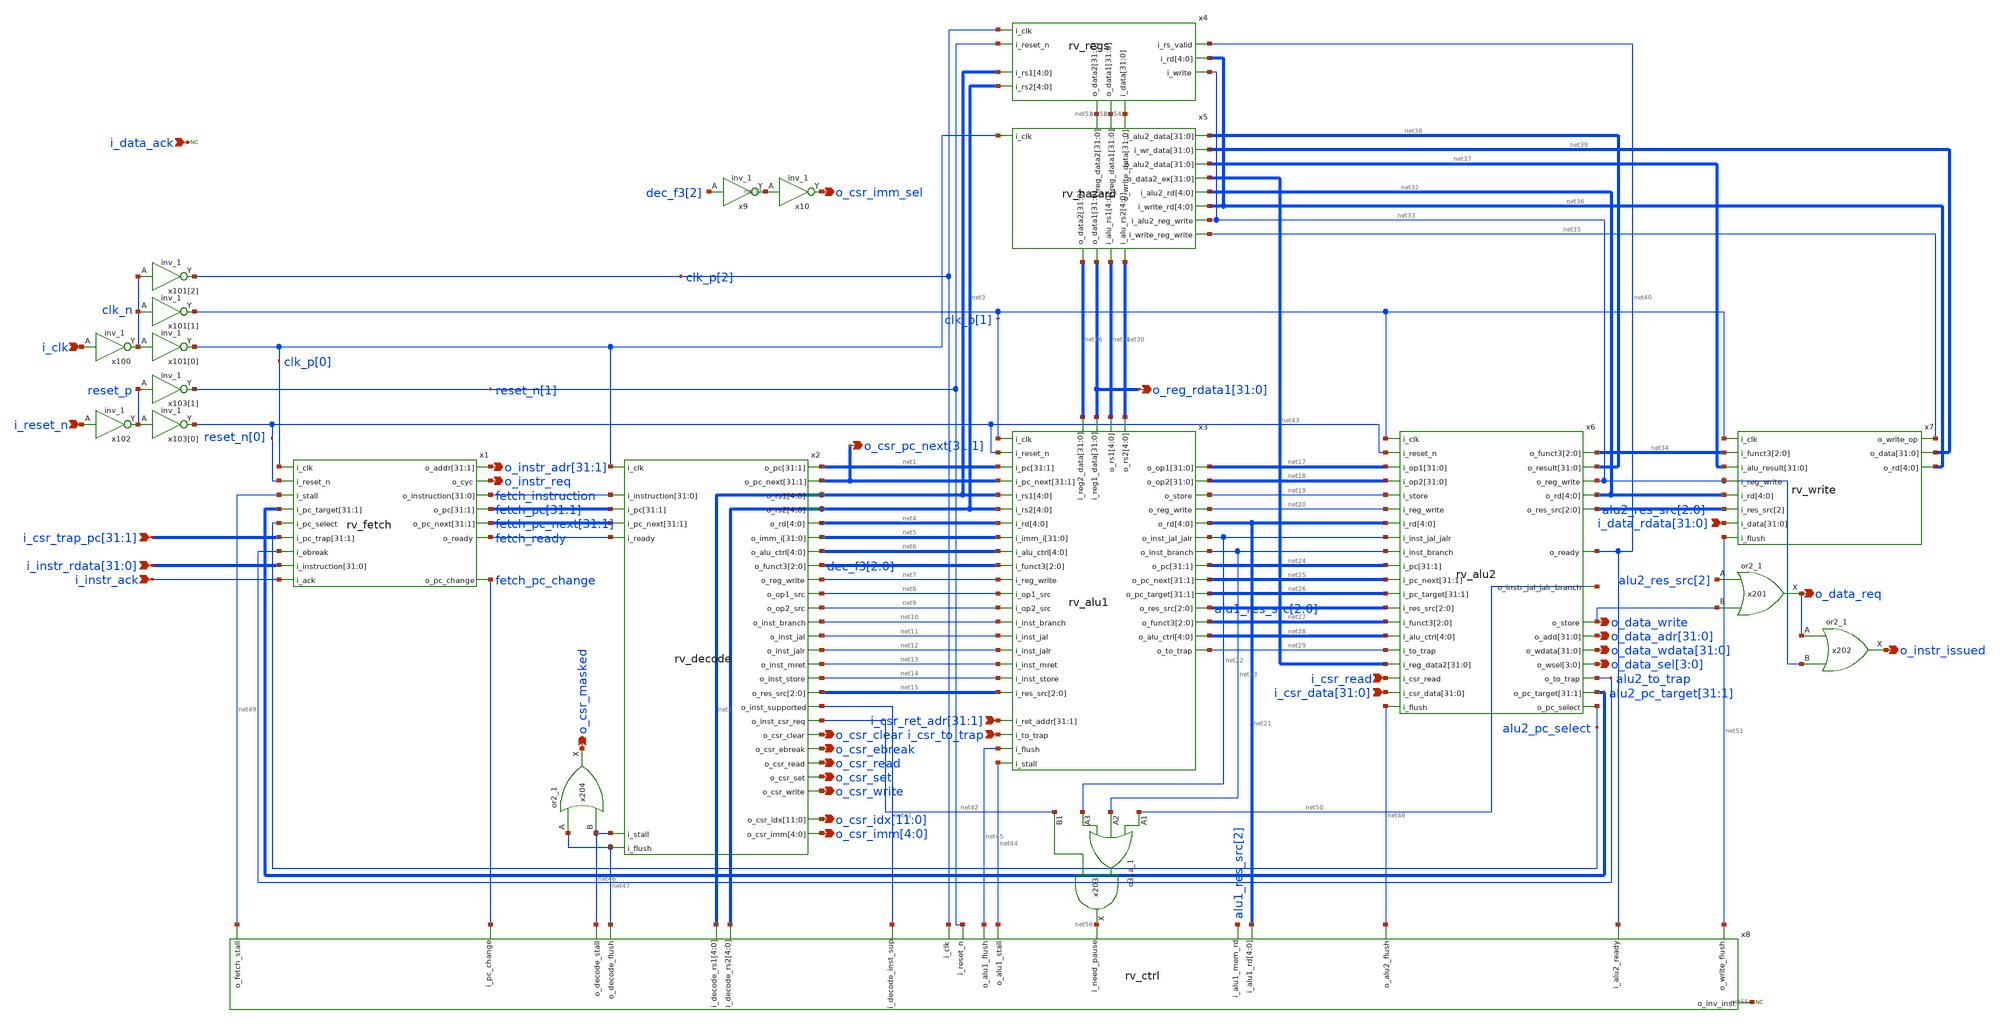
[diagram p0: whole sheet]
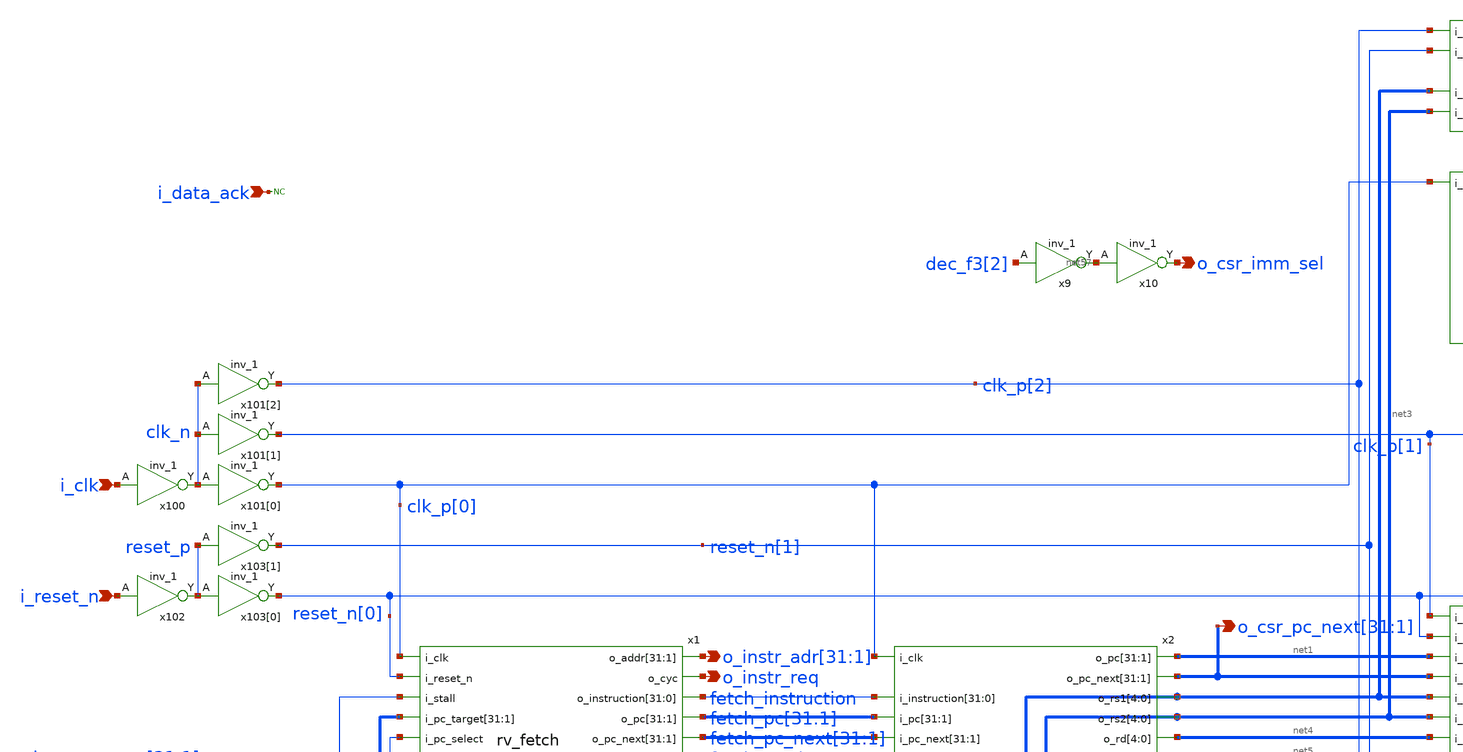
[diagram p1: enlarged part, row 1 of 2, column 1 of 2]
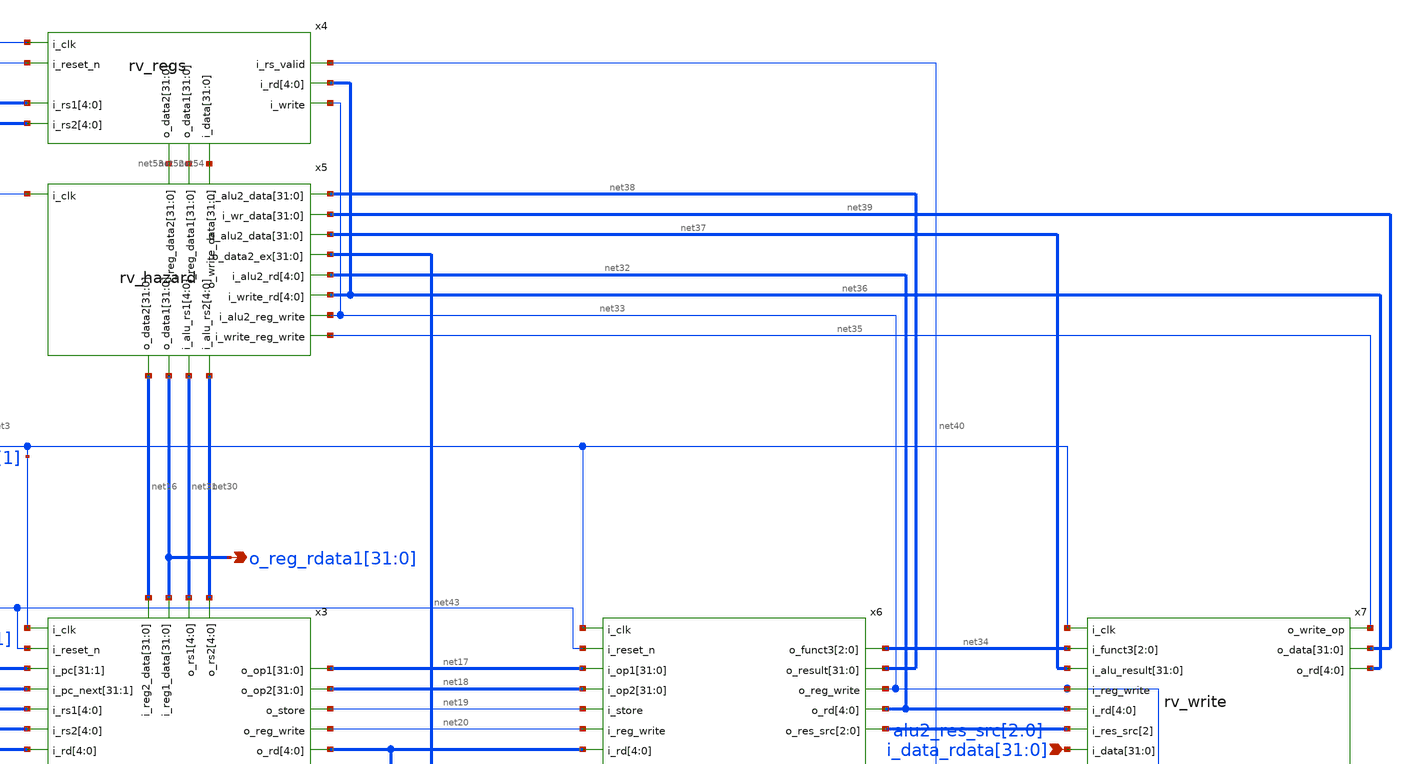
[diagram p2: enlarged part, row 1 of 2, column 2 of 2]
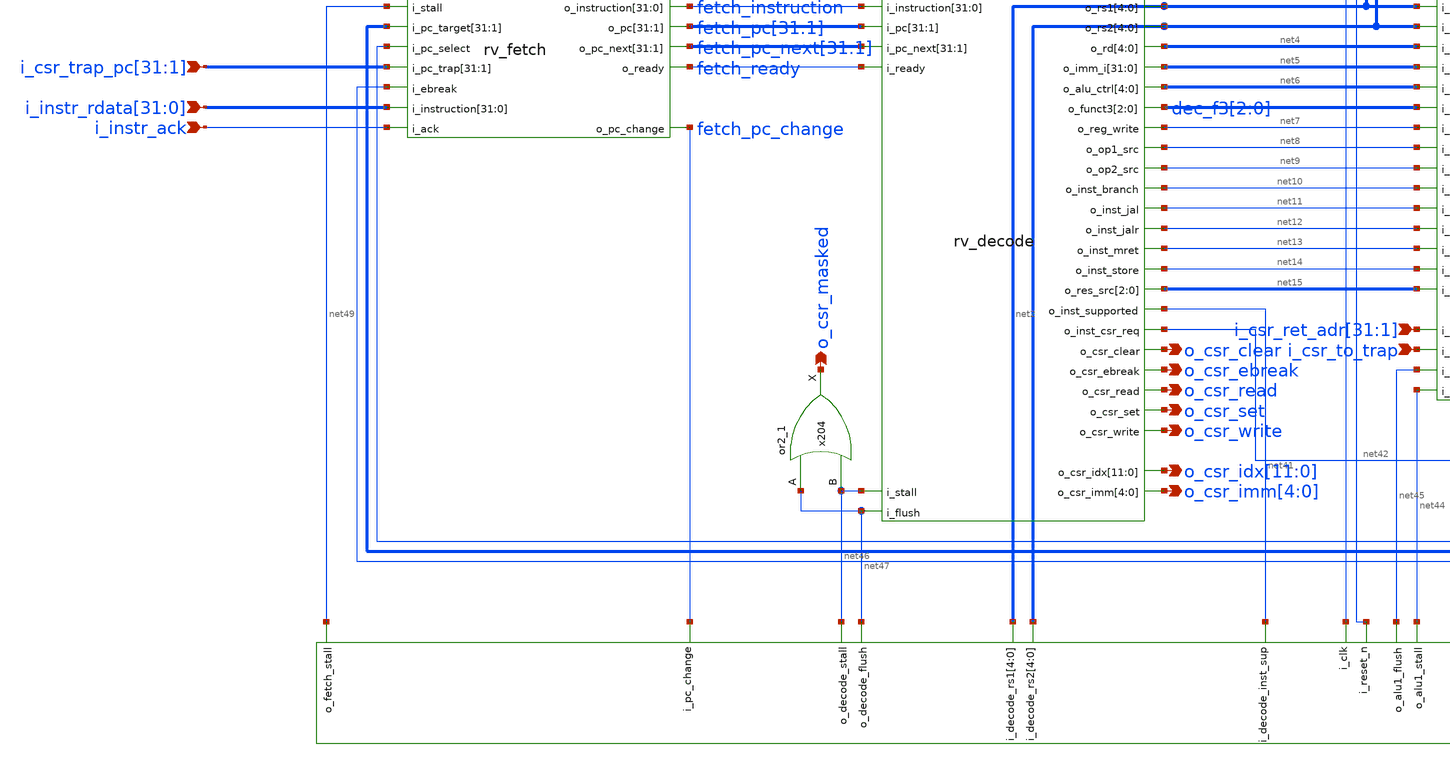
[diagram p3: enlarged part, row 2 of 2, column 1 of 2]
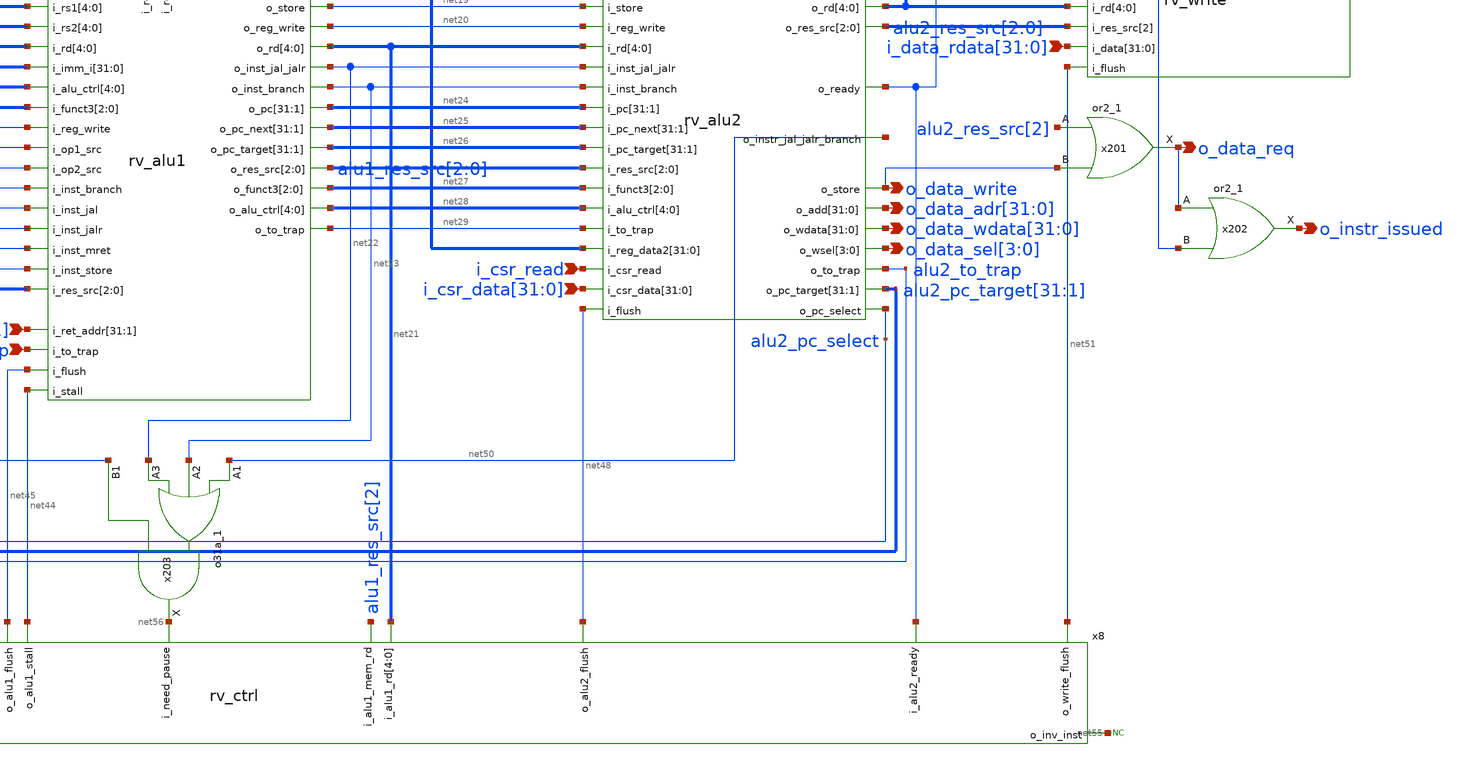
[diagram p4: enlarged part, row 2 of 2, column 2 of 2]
** sch_path: blocks/rv_core/rv_core.sch
**.subckt rv_core i_clk i_reset_n i_csr_read o_csr_clear o_data_req
*+ o_data_wdata[31],o_data_wdata[30],o_data_wdata[29],o_data_wdata[28],o_data_wdata[27],o_data_wdata[26],o_data_wdata[25],o_data_wdata[24],o_data_wdata[23],o_data_wdata[22],o_data_wdata[21],o_data_wdata[20],o_data_wdata[19],o_data_wdata[18],o_data_wdata[17],o_data_wdata[16],o_data_wdata[15],o_data_wdata[14],o_data_wdata[13],o_data_wdata[12],o_data_wdata[11],o_data_wdata[10],o_data_wdata[9],o_data_wdata[8],o_data_wdata[7],o_data_wdata[6],o_data_wdata[5],o_data_wdata[4],o_data_wdata[3],o_data_wdata[2],o_data_wdata[1],o_data_wdata[0] o_instr_issued
*+ o_data_adr[31],o_data_adr[30],o_data_adr[29],o_data_adr[28],o_data_adr[27],o_data_adr[26],o_data_adr[25],o_data_adr[24],o_data_adr[23],o_data_adr[22],o_data_adr[21],o_data_adr[20],o_data_adr[19],o_data_adr[18],o_data_adr[17],o_data_adr[16],o_data_adr[15],o_data_adr[14],o_data_adr[13],o_data_adr[12],o_data_adr[11],o_data_adr[10],o_data_adr[9],o_data_adr[8],o_data_adr[7],o_data_adr[6],o_data_adr[5],o_data_adr[4],o_data_adr[3],o_data_adr[2],o_data_adr[1],o_data_adr[0] o_data_sel[3],o_data_sel[2],o_data_sel[1],o_data_sel[0]
*+ i_csr_data[31],i_csr_data[30],i_csr_data[29],i_csr_data[28],i_csr_data[27],i_csr_data[26],i_csr_data[25],i_csr_data[24],i_csr_data[23],i_csr_data[22],i_csr_data[21],i_csr_data[20],i_csr_data[19],i_csr_data[18],i_csr_data[17],i_csr_data[16],i_csr_data[15],i_csr_data[14],i_csr_data[13],i_csr_data[12],i_csr_data[11],i_csr_data[10],i_csr_data[9],i_csr_data[8],i_csr_data[7],i_csr_data[6],i_csr_data[5],i_csr_data[4],i_csr_data[3],i_csr_data[2],i_csr_data[1],i_csr_data[0] i_csr_to_trap o_csr_ebreak o_csr_read o_csr_set o_csr_write o_csr_imm_sel
*+ i_csr_ret_adr[31],i_csr_ret_adr[30],i_csr_ret_adr[29],i_csr_ret_adr[28],i_csr_ret_adr[27],i_csr_ret_adr[26],i_csr_ret_adr[25],i_csr_ret_adr[24],i_csr_ret_adr[23],i_csr_ret_adr[22],i_csr_ret_adr[21],i_csr_ret_adr[20],i_csr_ret_adr[19],i_csr_ret_adr[18],i_csr_ret_adr[17],i_csr_ret_adr[16],i_csr_ret_adr[15],i_csr_ret_adr[14],i_csr_ret_adr[13],i_csr_ret_adr[12],i_csr_ret_adr[11],i_csr_ret_adr[10],i_csr_ret_adr[9],i_csr_ret_adr[8],i_csr_ret_adr[7],i_csr_ret_adr[6],i_csr_ret_adr[5],i_csr_ret_adr[4],i_csr_ret_adr[3],i_csr_ret_adr[2],i_csr_ret_adr[1]
*+ i_csr_trap_pc[31],i_csr_trap_pc[30],i_csr_trap_pc[29],i_csr_trap_pc[28],i_csr_trap_pc[27],i_csr_trap_pc[26],i_csr_trap_pc[25],i_csr_trap_pc[24],i_csr_trap_pc[23],i_csr_trap_pc[22],i_csr_trap_pc[21],i_csr_trap_pc[20],i_csr_trap_pc[19],i_csr_trap_pc[18],i_csr_trap_pc[17],i_csr_trap_pc[16],i_csr_trap_pc[15],i_csr_trap_pc[14],i_csr_trap_pc[13],i_csr_trap_pc[12],i_csr_trap_pc[11],i_csr_trap_pc[10],i_csr_trap_pc[9],i_csr_trap_pc[8],i_csr_trap_pc[7],i_csr_trap_pc[6],i_csr_trap_pc[5],i_csr_trap_pc[4],i_csr_trap_pc[3],i_csr_trap_pc[2],i_csr_trap_pc[1]
*+ o_csr_idx[11],o_csr_idx[10],o_csr_idx[9],o_csr_idx[8],o_csr_idx[7],o_csr_idx[6],o_csr_idx[5],o_csr_idx[4],o_csr_idx[3],o_csr_idx[2],o_csr_idx[1],o_csr_idx[0] o_csr_imm[4],o_csr_imm[3],o_csr_imm[2],o_csr_imm[1],o_csr_imm[0]
*+ o_csr_pc_next[31],o_csr_pc_next[30],o_csr_pc_next[29],o_csr_pc_next[28],o_csr_pc_next[27],o_csr_pc_next[26],o_csr_pc_next[25],o_csr_pc_next[24],o_csr_pc_next[23],o_csr_pc_next[22],o_csr_pc_next[21],o_csr_pc_next[20],o_csr_pc_next[19],o_csr_pc_next[18],o_csr_pc_next[17],o_csr_pc_next[16],o_csr_pc_next[15],o_csr_pc_next[14],o_csr_pc_next[13],o_csr_pc_next[12],o_csr_pc_next[11],o_csr_pc_next[10],o_csr_pc_next[9],o_csr_pc_next[8],o_csr_pc_next[7],o_csr_pc_next[6],o_csr_pc_next[5],o_csr_pc_next[4],o_csr_pc_next[3],o_csr_pc_next[2],o_csr_pc_next[1]
*+ o_reg_rdata1[31],o_reg_rdata1[30],o_reg_rdata1[29],o_reg_rdata1[28],o_reg_rdata1[27],o_reg_rdata1[26],o_reg_rdata1[25],o_reg_rdata1[24],o_reg_rdata1[23],o_reg_rdata1[22],o_reg_rdata1[21],o_reg_rdata1[20],o_reg_rdata1[19],o_reg_rdata1[18],o_reg_rdata1[17],o_reg_rdata1[16],o_reg_rdata1[15],o_reg_rdata1[14],o_reg_rdata1[13],o_reg_rdata1[12],o_reg_rdata1[11],o_reg_rdata1[10],o_reg_rdata1[9],o_reg_rdata1[8],o_reg_rdata1[7],o_reg_rdata1[6],o_reg_rdata1[5],o_reg_rdata1[4],o_reg_rdata1[3],o_reg_rdata1[2],o_reg_rdata1[1],o_reg_rdata1[0] i_data_ack o_data_write
*+ i_data_rdata[31],i_data_rdata[30],i_data_rdata[29],i_data_rdata[28],i_data_rdata[27],i_data_rdata[26],i_data_rdata[25],i_data_rdata[24],i_data_rdata[23],i_data_rdata[22],i_data_rdata[21],i_data_rdata[20],i_data_rdata[19],i_data_rdata[18],i_data_rdata[17],i_data_rdata[16],i_data_rdata[15],i_data_rdata[14],i_data_rdata[13],i_data_rdata[12],i_data_rdata[11],i_data_rdata[10],i_data_rdata[9],i_data_rdata[8],i_data_rdata[7],i_data_rdata[6],i_data_rdata[5],i_data_rdata[4],i_data_rdata[3],i_data_rdata[2],i_data_rdata[1],i_data_rdata[0] i_instr_ack o_instr_req
*+ i_instr_rdata[31],i_instr_rdata[30],i_instr_rdata[29],i_instr_rdata[28],i_instr_rdata[27],i_instr_rdata[26],i_instr_rdata[25],i_instr_rdata[24],i_instr_rdata[23],i_instr_rdata[22],i_instr_rdata[21],i_instr_rdata[20],i_instr_rdata[19],i_instr_rdata[18],i_instr_rdata[17],i_instr_rdata[16],i_instr_rdata[15],i_instr_rdata[14],i_instr_rdata[13],i_instr_rdata[12],i_instr_rdata[11],i_instr_rdata[10],i_instr_rdata[9],i_instr_rdata[8],i_instr_rdata[7],i_instr_rdata[6],i_instr_rdata[5],i_instr_rdata[4],i_instr_rdata[3],i_instr_rdata[2],i_instr_rdata[1],i_instr_rdata[0]
*+ o_instr_adr[31],o_instr_adr[30],o_instr_adr[29],o_instr_adr[28],o_instr_adr[27],o_instr_adr[26],o_instr_adr[25],o_instr_adr[24],o_instr_adr[23],o_instr_adr[22],o_instr_adr[21],o_instr_adr[20],o_instr_adr[19],o_instr_adr[18],o_instr_adr[17],o_instr_adr[16],o_instr_adr[15],o_instr_adr[14],o_instr_adr[13],o_instr_adr[12],o_instr_adr[11],o_instr_adr[10],o_instr_adr[9],o_instr_adr[8],o_instr_adr[7],o_instr_adr[6],o_instr_adr[5],o_instr_adr[4],o_instr_adr[3],o_instr_adr[2],o_instr_adr[1] o_csr_masked
*.ipin i_clk
*.ipin i_reset_n
*.ipin i_csr_read
*.opin o_csr_clear
*.opin o_data_req
*.opin
*+ o_data_wdata[31],o_data_wdata[30],o_data_wdata[29],o_data_wdata[28],o_data_wdata[27],o_data_wdata[26],o_data_wdata[25],o_data_wdata[24],o_data_wdata[23],o_data_wdata[22],o_data_wdata[21],o_data_wdata[20],o_data_wdata[19],o_data_wdata[18],o_data_wdata[17],o_data_wdata[16],o_data_wdata[15],o_data_wdata[14],o_data_wdata[13],o_data_wdata[12],o_data_wdata[11],o_data_wdata[10],o_data_wdata[9],o_data_wdata[8],o_data_wdata[7],o_data_wdata[6],o_data_wdata[5],o_data_wdata[4],o_data_wdata[3],o_data_wdata[2],o_data_wdata[1],o_data_wdata[0]
*.opin o_instr_issued
*.opin
*+ o_data_adr[31],o_data_adr[30],o_data_adr[29],o_data_adr[28],o_data_adr[27],o_data_adr[26],o_data_adr[25],o_data_adr[24],o_data_adr[23],o_data_adr[22],o_data_adr[21],o_data_adr[20],o_data_adr[19],o_data_adr[18],o_data_adr[17],o_data_adr[16],o_data_adr[15],o_data_adr[14],o_data_adr[13],o_data_adr[12],o_data_adr[11],o_data_adr[10],o_data_adr[9],o_data_adr[8],o_data_adr[7],o_data_adr[6],o_data_adr[5],o_data_adr[4],o_data_adr[3],o_data_adr[2],o_data_adr[1],o_data_adr[0]
*.opin o_data_sel[3],o_data_sel[2],o_data_sel[1],o_data_sel[0]
*.ipin
*+ i_csr_data[31],i_csr_data[30],i_csr_data[29],i_csr_data[28],i_csr_data[27],i_csr_data[26],i_csr_data[25],i_csr_data[24],i_csr_data[23],i_csr_data[22],i_csr_data[21],i_csr_data[20],i_csr_data[19],i_csr_data[18],i_csr_data[17],i_csr_data[16],i_csr_data[15],i_csr_data[14],i_csr_data[13],i_csr_data[12],i_csr_data[11],i_csr_data[10],i_csr_data[9],i_csr_data[8],i_csr_data[7],i_csr_data[6],i_csr_data[5],i_csr_data[4],i_csr_data[3],i_csr_data[2],i_csr_data[1],i_csr_data[0]
*.ipin i_csr_to_trap
*.opin o_csr_ebreak
*.opin o_csr_read
*.opin o_csr_set
*.opin o_csr_write
*.opin o_csr_imm_sel
*.ipin
*+ i_csr_ret_adr[31],i_csr_ret_adr[30],i_csr_ret_adr[29],i_csr_ret_adr[28],i_csr_ret_adr[27],i_csr_ret_adr[26],i_csr_ret_adr[25],i_csr_ret_adr[24],i_csr_ret_adr[23],i_csr_ret_adr[22],i_csr_ret_adr[21],i_csr_ret_adr[20],i_csr_ret_adr[19],i_csr_ret_adr[18],i_csr_ret_adr[17],i_csr_ret_adr[16],i_csr_ret_adr[15],i_csr_ret_adr[14],i_csr_ret_adr[13],i_csr_ret_adr[12],i_csr_ret_adr[11],i_csr_ret_adr[10],i_csr_ret_adr[9],i_csr_ret_adr[8],i_csr_ret_adr[7],i_csr_ret_adr[6],i_csr_ret_adr[5],i_csr_ret_adr[4],i_csr_ret_adr[3],i_csr_ret_adr[2],i_csr_ret_adr[1]
*.ipin
*+ i_csr_trap_pc[31],i_csr_trap_pc[30],i_csr_trap_pc[29],i_csr_trap_pc[28],i_csr_trap_pc[27],i_csr_trap_pc[26],i_csr_trap_pc[25],i_csr_trap_pc[24],i_csr_trap_pc[23],i_csr_trap_pc[22],i_csr_trap_pc[21],i_csr_trap_pc[20],i_csr_trap_pc[19],i_csr_trap_pc[18],i_csr_trap_pc[17],i_csr_trap_pc[16],i_csr_trap_pc[15],i_csr_trap_pc[14],i_csr_trap_pc[13],i_csr_trap_pc[12],i_csr_trap_pc[11],i_csr_trap_pc[10],i_csr_trap_pc[9],i_csr_trap_pc[8],i_csr_trap_pc[7],i_csr_trap_pc[6],i_csr_trap_pc[5],i_csr_trap_pc[4],i_csr_trap_pc[3],i_csr_trap_pc[2],i_csr_trap_pc[1]
*.opin
*+ o_csr_idx[11],o_csr_idx[10],o_csr_idx[9],o_csr_idx[8],o_csr_idx[7],o_csr_idx[6],o_csr_idx[5],o_csr_idx[4],o_csr_idx[3],o_csr_idx[2],o_csr_idx[1],o_csr_idx[0]
*.opin o_csr_imm[4],o_csr_imm[3],o_csr_imm[2],o_csr_imm[1],o_csr_imm[0]
*.opin
*+ o_csr_pc_next[31],o_csr_pc_next[30],o_csr_pc_next[29],o_csr_pc_next[28],o_csr_pc_next[27],o_csr_pc_next[26],o_csr_pc_next[25],o_csr_pc_next[24],o_csr_pc_next[23],o_csr_pc_next[22],o_csr_pc_next[21],o_csr_pc_next[20],o_csr_pc_next[19],o_csr_pc_next[18],o_csr_pc_next[17],o_csr_pc_next[16],o_csr_pc_next[15],o_csr_pc_next[14],o_csr_pc_next[13],o_csr_pc_next[12],o_csr_pc_next[11],o_csr_pc_next[10],o_csr_pc_next[9],o_csr_pc_next[8],o_csr_pc_next[7],o_csr_pc_next[6],o_csr_pc_next[5],o_csr_pc_next[4],o_csr_pc_next[3],o_csr_pc_next[2],o_csr_pc_next[1]
*.opin
*+ o_reg_rdata1[31],o_reg_rdata1[30],o_reg_rdata1[29],o_reg_rdata1[28],o_reg_rdata1[27],o_reg_rdata1[26],o_reg_rdata1[25],o_reg_rdata1[24],o_reg_rdata1[23],o_reg_rdata1[22],o_reg_rdata1[21],o_reg_rdata1[20],o_reg_rdata1[19],o_reg_rdata1[18],o_reg_rdata1[17],o_reg_rdata1[16],o_reg_rdata1[15],o_reg_rdata1[14],o_reg_rdata1[13],o_reg_rdata1[12],o_reg_rdata1[11],o_reg_rdata1[10],o_reg_rdata1[9],o_reg_rdata1[8],o_reg_rdata1[7],o_reg_rdata1[6],o_reg_rdata1[5],o_reg_rdata1[4],o_reg_rdata1[3],o_reg_rdata1[2],o_reg_rdata1[1],o_reg_rdata1[0]
*.ipin i_data_ack
*.opin o_data_write
*.ipin
*+ i_data_rdata[31],i_data_rdata[30],i_data_rdata[29],i_data_rdata[28],i_data_rdata[27],i_data_rdata[26],i_data_rdata[25],i_data_rdata[24],i_data_rdata[23],i_data_rdata[22],i_data_rdata[21],i_data_rdata[20],i_data_rdata[19],i_data_rdata[18],i_data_rdata[17],i_data_rdata[16],i_data_rdata[15],i_data_rdata[14],i_data_rdata[13],i_data_rdata[12],i_data_rdata[11],i_data_rdata[10],i_data_rdata[9],i_data_rdata[8],i_data_rdata[7],i_data_rdata[6],i_data_rdata[5],i_data_rdata[4],i_data_rdata[3],i_data_rdata[2],i_data_rdata[1],i_data_rdata[0]
*.ipin i_instr_ack
*.opin o_instr_req
*.ipin
*+ i_instr_rdata[31],i_instr_rdata[30],i_instr_rdata[29],i_instr_rdata[28],i_instr_rdata[27],i_instr_rdata[26],i_instr_rdata[25],i_instr_rdata[24],i_instr_rdata[23],i_instr_rdata[22],i_instr_rdata[21],i_instr_rdata[20],i_instr_rdata[19],i_instr_rdata[18],i_instr_rdata[17],i_instr_rdata[16],i_instr_rdata[15],i_instr_rdata[14],i_instr_rdata[13],i_instr_rdata[12],i_instr_rdata[11],i_instr_rdata[10],i_instr_rdata[9],i_instr_rdata[8],i_instr_rdata[7],i_instr_rdata[6],i_instr_rdata[5],i_instr_rdata[4],i_instr_rdata[3],i_instr_rdata[2],i_instr_rdata[1],i_instr_rdata[0]
*.opin
*+ o_instr_adr[31],o_instr_adr[30],o_instr_adr[29],o_instr_adr[28],o_instr_adr[27],o_instr_adr[26],o_instr_adr[25],o_instr_adr[24],o_instr_adr[23],o_instr_adr[22],o_instr_adr[21],o_instr_adr[20],o_instr_adr[19],o_instr_adr[18],o_instr_adr[17],o_instr_adr[16],o_instr_adr[15],o_instr_adr[14],o_instr_adr[13],o_instr_adr[12],o_instr_adr[11],o_instr_adr[10],o_instr_adr[9],o_instr_adr[8],o_instr_adr[7],o_instr_adr[6],o_instr_adr[5],o_instr_adr[4],o_instr_adr[3],o_instr_adr[2],o_instr_adr[1]
*.opin o_csr_masked
x1 fetch_pc_change clk_p[0] reset_n[0] o_instr_adr[31] o_instr_adr[30] o_instr_adr[29]
+ o_instr_adr[28] o_instr_adr[27] o_instr_adr[26] o_instr_adr[25] o_instr_adr[24] o_instr_adr[23] o_instr_adr[22]
+ o_instr_adr[21] o_instr_adr[20] o_instr_adr[19] o_instr_adr[18] o_instr_adr[17] o_instr_adr[16] o_instr_adr[15]
+ o_instr_adr[14] o_instr_adr[13] o_instr_adr[12] o_instr_adr[11] o_instr_adr[10] o_instr_adr[9] o_instr_adr[8]
+ o_instr_adr[7] o_instr_adr[6] o_instr_adr[5] o_instr_adr[4] o_instr_adr[3] o_instr_adr[2] o_instr_adr[1]
+ o_instr_req net49 fetch_instruction fetch_instruction fetch_instruction fetch_instruction fetch_instruction
+ fetch_instruction fetch_instruction fetch_instruction fetch_instruction fetch_instruction fetch_instruction
+ fetch_instruction fetch_instruction fetch_instruction fetch_instruction fetch_instruction fetch_instruction
+ fetch_instruction fetch_instruction fetch_instruction fetch_instruction fetch_instruction fetch_instruction
+ fetch_instruction fetch_instruction fetch_instruction fetch_instruction fetch_instruction fetch_instruction
+ fetch_instruction fetch_instruction fetch_instruction alu2_pc_target[31] alu2_pc_target[30] alu2_pc_target[29]
+ alu2_pc_target[28] alu2_pc_target[27] alu2_pc_target[26] alu2_pc_target[25] alu2_pc_target[24] alu2_pc_target[23]
+ alu2_pc_target[22] alu2_pc_target[21] alu2_pc_target[20] alu2_pc_target[19] alu2_pc_target[18] alu2_pc_target[17]
+ alu2_pc_target[16] alu2_pc_target[15] alu2_pc_target[14] alu2_pc_target[13] alu2_pc_target[12] alu2_pc_target[11]
+ alu2_pc_target[10] alu2_pc_target[9] alu2_pc_target[8] alu2_pc_target[7] alu2_pc_target[6] alu2_pc_target[5]
+ alu2_pc_target[4] alu2_pc_target[3] alu2_pc_target[2] alu2_pc_target[1] alu2_pc_select fetch_pc[31] fetch_pc[30]
+ fetch_pc[29] fetch_pc[28] fetch_pc[27] fetch_pc[26] fetch_pc[25] fetch_pc[24] fetch_pc[23] fetch_pc[22]
+ fetch_pc[21] fetch_pc[20] fetch_pc[19] fetch_pc[18] fetch_pc[17] fetch_pc[16] fetch_pc[15] fetch_pc[14]
+ fetch_pc[13] fetch_pc[12] fetch_pc[11] fetch_pc[10] fetch_pc[9] fetch_pc[8] fetch_pc[7] fetch_pc[6] fetch_pc[5]
+ fetch_pc[4] fetch_pc[3] fetch_pc[2] fetch_pc[1] fetch_pc_next[31] fetch_pc_next[30] fetch_pc_next[29]
+ fetch_pc_next[28] fetch_pc_next[27] fetch_pc_next[26] fetch_pc_next[25] fetch_pc_next[24] fetch_pc_next[23]
+ fetch_pc_next[22] fetch_pc_next[21] fetch_pc_next[20] fetch_pc_next[19] fetch_pc_next[18] fetch_pc_next[17]
+ fetch_pc_next[16] fetch_pc_next[15] fetch_pc_next[14] fetch_pc_next[13] fetch_pc_next[12] fetch_pc_next[11]
+ fetch_pc_next[10] fetch_pc_next[9] fetch_pc_next[8] fetch_pc_next[7] fetch_pc_next[6] fetch_pc_next[5]
+ fetch_pc_next[4] fetch_pc_next[3] fetch_pc_next[2] fetch_pc_next[1] i_csr_trap_pc[31] i_csr_trap_pc[30]
+ i_csr_trap_pc[29] i_csr_trap_pc[28] i_csr_trap_pc[27] i_csr_trap_pc[26] i_csr_trap_pc[25] i_csr_trap_pc[24]
+ i_csr_trap_pc[23] i_csr_trap_pc[22] i_csr_trap_pc[21] i_csr_trap_pc[20] i_csr_trap_pc[19] i_csr_trap_pc[18]
+ i_csr_trap_pc[17] i_csr_trap_pc[16] i_csr_trap_pc[15] i_csr_trap_pc[14] i_csr_trap_pc[13] i_csr_trap_pc[12]
+ i_csr_trap_pc[11] i_csr_trap_pc[10] i_csr_trap_pc[9] i_csr_trap_pc[8] i_csr_trap_pc[7] i_csr_trap_pc[6]
+ i_csr_trap_pc[5] i_csr_trap_pc[4] i_csr_trap_pc[3] i_csr_trap_pc[2] i_csr_trap_pc[1] fetch_ready alu2_to_trap
+ i_instr_rdata[31] i_instr_rdata[30] i_instr_rdata[29] i_instr_rdata[28] i_instr_rdata[27] i_instr_rdata[26]
+ i_instr_rdata[25] i_instr_rdata[24] i_instr_rdata[23] i_instr_rdata[22] i_instr_rdata[21] i_instr_rdata[20]
+ i_instr_rdata[19] i_instr_rdata[18] i_instr_rdata[17] i_instr_rdata[16] i_instr_rdata[15] i_instr_rdata[14]
+ i_instr_rdata[13] i_instr_rdata[12] i_instr_rdata[11] i_instr_rdata[10] i_instr_rdata[9] i_instr_rdata[8]
+ i_instr_rdata[7] i_instr_rdata[6] i_instr_rdata[5] i_instr_rdata[4] i_instr_rdata[3] i_instr_rdata[2]
+ i_instr_rdata[1] i_instr_rdata[0] i_instr_ack rv_fetch
x100 i_clk VSS VSS VCC VCC clk_n sky130_fd_sc_hd__inv_1
x102 i_reset_n VSS VSS VCC VCC reset_p sky130_fd_sc_hd__inv_1
x103[0] reset_p VSS VSS VCC VCC reset_n[0] sky130_fd_sc_hd__inv_1
x101[2] clk_n VSS VSS VCC VCC clk_p[2] sky130_fd_sc_hd__inv_1
x101[1] clk_n VSS VSS VCC VCC clk_p[1] sky130_fd_sc_hd__inv_1
x101[0] clk_n VSS VSS VCC VCC clk_p[0] sky130_fd_sc_hd__inv_1
x103[1] reset_p VSS VSS VCC VCC reset_n[1] sky130_fd_sc_hd__inv_1
x2 net1[30] net1[29] net1[28] net1[27] net1[26] net1[25] net1[24] net1[23] net1[22] net1[21]
+ net1[20] net1[19] net1[18] net1[17] net1[16] net1[15] net1[14] net1[13] net1[12] net1[11] net1[10] net1[9]
+ net1[8] net1[7] net1[6] net1[5] net1[4] net1[3] net1[2] net1[1] net1[0] clk_p[0] net46 o_csr_pc_next[31]
+ o_csr_pc_next[30] o_csr_pc_next[29] o_csr_pc_next[28] o_csr_pc_next[27] o_csr_pc_next[26] o_csr_pc_next[25]
+ o_csr_pc_next[24] o_csr_pc_next[23] o_csr_pc_next[22] o_csr_pc_next[21] o_csr_pc_next[20] o_csr_pc_next[19]
+ o_csr_pc_next[18] o_csr_pc_next[17] o_csr_pc_next[16] o_csr_pc_next[15] o_csr_pc_next[14] o_csr_pc_next[13]
+ o_csr_pc_next[12] o_csr_pc_next[11] o_csr_pc_next[10] o_csr_pc_next[9] o_csr_pc_next[8] o_csr_pc_next[7]
+ o_csr_pc_next[6] o_csr_pc_next[5] o_csr_pc_next[4] o_csr_pc_next[3] o_csr_pc_next[2] o_csr_pc_next[1] net47 net2[4]
+ net2[3] net2[2] net2[1] net2[0] fetch_instruction fetch_instruction fetch_instruction fetch_instruction
+ fetch_instruction fetch_instruction fetch_instruction fetch_instruction fetch_instruction fetch_instruction
+ fetch_instruction fetch_instruction fetch_instruction fetch_instruction fetch_instruction fetch_instruction
+ fetch_instruction fetch_instruction fetch_instruction fetch_instruction fetch_instruction fetch_instruction
+ fetch_instruction fetch_instruction fetch_instruction fetch_instruction fetch_instruction fetch_instruction
+ fetch_instruction fetch_instruction fetch_instruction fetch_instruction net3[4] net3[3] net3[2] net3[1] net3[0]
+ net4[4] net4[3] net4[2] net4[1] net4[0] fetch_pc[31] fetch_pc[30] fetch_pc[29] fetch_pc[28] fetch_pc[27]
+ fetch_pc[26] fetch_pc[25] fetch_pc[24] fetch_pc[23] fetch_pc[22] fetch_pc[21] fetch_pc[20] fetch_pc[19]
+ fetch_pc[18] fetch_pc[17] fetch_pc[16] fetch_pc[15] fetch_pc[14] fetch_pc[13] fetch_pc[12] fetch_pc[11]
+ fetch_pc[10] fetch_pc[9] fetch_pc[8] fetch_pc[7] fetch_pc[6] fetch_pc[5] fetch_pc[4] fetch_pc[3] fetch_pc[2]
+ fetch_pc[1] net5[31] net5[30] net5[29] net5[28] net5[27] net5[26] net5[25] net5[24] net5[23] net5[22] net5[21]
+ net5[20] net5[19] net5[18] net5[17] net5[16] net5[15] net5[14] net5[13] net5[12] net5[11] net5[10] net5[9]
+ net5[8] net5[7] net5[6] net5[5] net5[4] net5[3] net5[2] net5[1] net5[0] fetch_pc_next[31] fetch_pc_next[30]
+ fetch_pc_next[29] fetch_pc_next[28] fetch_pc_next[27] fetch_pc_next[26] fetch_pc_next[25] fetch_pc_next[24]
+ fetch_pc_next[23] fetch_pc_next[22] fetch_pc_next[21] fetch_pc_next[20] fetch_pc_next[19] fetch_pc_next[18]
+ fetch_pc_next[17] fetch_pc_next[16] fetch_pc_next[15] fetch_pc_next[14] fetch_pc_next[13] fetch_pc_next[12]
+ fetch_pc_next[11] fetch_pc_next[10] fetch_pc_next[9] fetch_pc_next[8] fetch_pc_next[7] fetch_pc_next[6]
+ fetch_pc_next[5] fetch_pc_next[4] fetch_pc_next[3] fetch_pc_next[2] fetch_pc_next[1] fetch_ready net6[4] net6[3]
+ net6[2] net6[1] net6[0] dec_f3[2] dec_f3[1] dec_f3[0] net7 net8 net9 net10 net42 net11 net12 net13 net14
+ net41 net15[2] net15[1] net15[0] o_csr_clear o_csr_ebreak o_csr_read o_csr_set o_csr_write o_csr_idx[11]
+ o_csr_idx[10] o_csr_idx[9] o_csr_idx[8] o_csr_idx[7] o_csr_idx[6] o_csr_idx[5] o_csr_idx[4] o_csr_idx[3]
+ o_csr_idx[2] o_csr_idx[1] o_csr_idx[0] o_csr_imm[4] o_csr_imm[3] o_csr_imm[2] o_csr_imm[1] o_csr_imm[0]
+ rv_decode
x3 clk_p[1] net17[31] net17[30] net17[29] net17[28] net17[27] net17[26] net17[25] net17[24]
+ net17[23] net17[22] net17[21] net17[20] net17[19] net17[18] net17[17] net17[16] net17[15] net17[14] net17[13]
+ net17[12] net17[11] net17[10] net17[9] net17[8] net17[7] net17[6] net17[5] net17[4] net17[3] net17[2]
+ net17[1] net17[0] reset_n[0] net18[31] net18[30] net18[29] net18[28] net18[27] net18[26] net18[25] net18[24]
+ net18[23] net18[22] net18[21] net18[20] net18[19] net18[18] net18[17] net18[16] net18[15] net18[14] net18[13]
+ net18[12] net18[11] net18[10] net18[9] net18[8] net18[7] net18[6] net18[5] net18[4] net18[3] net18[2]
+ net18[1] net18[0] net1[30] net1[29] net1[28] net1[27] net1[26] net1[25] net1[24] net1[23] net1[22] net1[21]
+ net1[20] net1[19] net1[18] net1[17] net1[16] net1[15] net1[14] net1[13] net1[12] net1[11] net1[10] net1[9]
+ net1[8] net1[7] net1[6] net1[5] net1[4] net1[3] net1[2] net1[1] net1[0] net19 net20 o_csr_pc_next[31]
+ o_csr_pc_next[30] o_csr_pc_next[29] o_csr_pc_next[28] o_csr_pc_next[27] o_csr_pc_next[26] o_csr_pc_next[25]
+ o_csr_pc_next[24] o_csr_pc_next[23] o_csr_pc_next[22] o_csr_pc_next[21] o_csr_pc_next[20] o_csr_pc_next[19]
+ o_csr_pc_next[18] o_csr_pc_next[17] o_csr_pc_next[16] o_csr_pc_next[15] o_csr_pc_next[14] o_csr_pc_next[13]
+ o_csr_pc_next[12] o_csr_pc_next[11] o_csr_pc_next[10] o_csr_pc_next[9] o_csr_pc_next[8] o_csr_pc_next[7]
+ o_csr_pc_next[6] o_csr_pc_next[5] o_csr_pc_next[4] o_csr_pc_next[3] o_csr_pc_next[2] o_csr_pc_next[1] net31[4]
+ net31[3] net31[2] net31[1] net31[0] net2[4] net2[3] net2[2] net2[1] net2[0] net3[4] net3[3] net3[2] net3[1]
+ net3[0] net30[4] net30[3] net30[2] net30[1] net30[0] net4[4] net4[3] net4[2] net4[1] net4[0] net21[4]
+ net21[3] net21[2] net21[1] net21[0] net5[31] net5[30] net5[29] net5[28] net5[27] net5[26] net5[25] net5[24]
+ net5[23] net5[22] net5[21] net5[20] net5[19] net5[18] net5[17] net5[16] net5[15] net5[14] net5[13] net5[12]
+ net5[11] net5[10] net5[9] net5[8] net5[7] net5[6] net5[5] net5[4] net5[3] net5[2] net5[1] net5[0] net22
+ net6[4] net6[3] net6[2] net6[1] net6[0] net23 dec_f3[2] dec_f3[1] dec_f3[0] net24[30] net24[29] net24[28]
+ net24[27] net24[26] net24[25] net24[24] net24[23] net24[22] net24[21] net24[20] net24[19] net24[18] net24[17]
+ net24[16] net24[15] net24[14] net24[13] net24[12] net24[11] net24[10] net24[9] net24[8] net24[7] net24[6]
+ net24[5] net24[4] net24[3] net24[2] net24[1] net24[0] net25[30] net25[29] net25[28] net25[27] net25[26]
+ net25[25] net25[24] net25[23] net25[22] net25[21] net25[20] net25[19] net25[18] net25[17] net25[16] net25[15]
+ net25[14] net25[13] net25[12] net25[11] net25[10] net25[9] net25[8] net25[7] net25[6] net25[5] net25[4]
+ net25[3] net25[2] net25[1] net25[0] net7 net26[30] net26[29] net26[28] net26[27] net26[26] net26[25]
+ net26[24] net26[23] net26[22] net26[21] net26[20] net26[19] net26[18] net26[17] net26[16] net26[15] net26[14]
+ net26[13] net26[12] net26[11] net26[10] net26[9] net26[8] net26[7] net26[6] net26[5] net26[4] net26[3]
+ net26[2] net26[1] net26[0] net8 net9 alu1_res_src[2] alu1_res_src[1] alu1_res_src[0] net10 net27[2] net27[1]
+ net27[0] net28[4] net28[3] net28[2] net28[1] net28[0] net11 net29 net12 net13 net14 net15[2] net15[1]
+ net15[0] o_reg_rdata1[31] o_reg_rdata1[30] o_reg_rdata1[29] o_reg_rdata1[28] o_reg_rdata1[27]
+ o_reg_rdata1[26] o_reg_rdata1[25] o_reg_rdata1[24] o_reg_rdata1[23] o_reg_rdata1[22] o_reg_rdata1[21]
+ o_reg_rdata1[20] o_reg_rdata1[19] o_reg_rdata1[18] o_reg_rdata1[17] o_reg_rdata1[16] o_reg_rdata1[15]
+ o_reg_rdata1[14] o_reg_rdata1[13] o_reg_rdata1[12] o_reg_rdata1[11] o_reg_rdata1[10] o_reg_rdata1[9] o_reg_rdata1[8]
+ o_reg_rdata1[7] o_reg_rdata1[6] o_reg_rdata1[5] o_reg_rdata1[4] o_reg_rdata1[3] o_reg_rdata1[2] o_reg_rdata1[1]
+ o_reg_rdata1[0] net16[31] net16[30] net16[29] net16[28] net16[27] net16[26] net16[25] net16[24] net16[23] net16[22]
+ net16[21] net16[20] net16[19] net16[18] net16[17] net16[16] net16[15] net16[14] net16[13] net16[12] net16[11]
+ net16[10] net16[9] net16[8] net16[7] net16[6] net16[5] net16[4] net16[3] net16[2] net16[1] net16[0]
+ i_csr_to_trap net45 net44 i_csr_ret_adr[31] i_csr_ret_adr[30] i_csr_ret_adr[29] i_csr_ret_adr[28]
+ i_csr_ret_adr[27] i_csr_ret_adr[26] i_csr_ret_adr[25] i_csr_ret_adr[24] i_csr_ret_adr[23] i_csr_ret_adr[22]
+ i_csr_ret_adr[21] i_csr_ret_adr[20] i_csr_ret_adr[19] i_csr_ret_adr[18] i_csr_ret_adr[17] i_csr_ret_adr[16]
+ i_csr_ret_adr[15] i_csr_ret_adr[14] i_csr_ret_adr[13] i_csr_ret_adr[12] i_csr_ret_adr[11] i_csr_ret_adr[10]
+ i_csr_ret_adr[9] i_csr_ret_adr[8] i_csr_ret_adr[7] i_csr_ret_adr[6] i_csr_ret_adr[5] i_csr_ret_adr[4]
+ i_csr_ret_adr[3] i_csr_ret_adr[2] i_csr_ret_adr[1] rv_alu1
x4 net52[31] net52[30] net52[29] net52[28] net52[27] net52[26] net52[25] net52[24] net52[23]
+ net52[22] net52[21] net52[20] net52[19] net52[18] net52[17] net52[16] net52[15] net52[14] net52[13] net52[12]
+ net52[11] net52[10] net52[9] net52[8] net52[7] net52[6] net52[5] net52[4] net52[3] net52[2] net52[1] net52[0]
+ clk_p[2] reset_n[1] net53[31] net53[30] net53[29] net53[28] net53[27] net53[26] net53[25] net53[24]
+ net53[23] net53[22] net53[21] net53[20] net53[19] net53[18] net53[17] net53[16] net53[15] net53[14] net53[13]
+ net53[12] net53[11] net53[10] net53[9] net53[8] net53[7] net53[6] net53[5] net53[4] net53[3] net53[2]
+ net53[1] net53[0] net40 net33 net2[4] net2[3] net2[2] net2[1] net2[0] net3[4] net3[3] net3[2] net3[1]
+ net3[0] net36[4] net36[3] net36[2] net36[1] net36[0] net54[31] net54[30] net54[29] net54[28] net54[27]
+ net54[26] net54[25] net54[24] net54[23] net54[22] net54[21] net54[20] net54[19] net54[18] net54[17] net54[16]
+ net54[15] net54[14] net54[13] net54[12] net54[11] net54[10] net54[9] net54[8] net54[7] net54[6] net54[5]
+ net54[4] net54[3] net54[2] net54[1] net54[0] rv_regs
x5 clk_p[0] o_reg_rdata1[31] o_reg_rdata1[30] o_reg_rdata1[29] o_reg_rdata1[28] o_reg_rdata1[27]
+ o_reg_rdata1[26] o_reg_rdata1[25] o_reg_rdata1[24] o_reg_rdata1[23] o_reg_rdata1[22] o_reg_rdata1[21]
+ o_reg_rdata1[20] o_reg_rdata1[19] o_reg_rdata1[18] o_reg_rdata1[17] o_reg_rdata1[16] o_reg_rdata1[15]
+ o_reg_rdata1[14] o_reg_rdata1[13] o_reg_rdata1[12] o_reg_rdata1[11] o_reg_rdata1[10] o_reg_rdata1[9] o_reg_rdata1[8]
+ o_reg_rdata1[7] o_reg_rdata1[6] o_reg_rdata1[5] o_reg_rdata1[4] o_reg_rdata1[3] o_reg_rdata1[2] o_reg_rdata1[1]
+ o_reg_rdata1[0] net31[4] net31[3] net31[2] net31[1] net31[0] net16[31] net16[30] net16[29] net16[28] net16[27]
+ net16[26] net16[25] net16[24] net16[23] net16[22] net16[21] net16[20] net16[19] net16[18] net16[17] net16[16]
+ net16[15] net16[14] net16[13] net16[12] net16[11] net16[10] net16[9] net16[8] net16[7] net16[6] net16[5]
+ net16[4] net16[3] net16[2] net16[1] net16[0] net30[4] net30[3] net30[2] net30[1] net30[0] net37[31]
+ net37[30] net37[29] net37[28] net37[27] net37[26] net37[25] net37[24] net37[23] net37[22] net37[21] net37[20]
+ net37[19] net37[18] net37[17] net37[16] net37[15] net37[14] net37[13] net37[12] net37[11] net37[10] net37[9]
+ net37[8] net37[7] net37[6] net37[5] net37[4] net37[3] net37[2] net37[1] net37[0] net32[4] net32[3] net32[2]
+ net32[1] net32[0] net54[31] net54[30] net54[29] net54[28] net54[27] net54[26] net54[25] net54[24] net54[23]
+ net54[22] net54[21] net54[20] net54[19] net54[18] net54[17] net54[16] net54[15] net54[14] net54[13] net54[12]
+ net54[11] net54[10] net54[9] net54[8] net54[7] net54[6] net54[5] net54[4] net54[3] net54[2] net54[1] net54[0]
+ net36[4] net36[3] net36[2] net36[1] net36[0] net43[31] net43[30] net43[29] net43[28] net43[27] net43[26]
+ net43[25] net43[24] net43[23] net43[22] net43[21] net43[20] net43[19] net43[18] net43[17] net43[16] net43[15]
+ net43[14] net43[13] net43[12] net43[11] net43[10] net43[9] net43[8] net43[7] net43[6] net43[5] net43[4]
+ net43[3] net43[2] net43[1] net43[0] net33 net35 net52[31] net52[30] net52[29] net52[28] net52[27] net52[26]
+ net52[25] net52[24] net52[23] net52[22] net52[21] net52[20] net52[19] net52[18] net52[17] net52[16] net52[15]
+ net52[14] net52[13] net52[12] net52[11] net52[10] net52[9] net52[8] net52[7] net52[6] net52[5] net52[4]
+ net52[3] net52[2] net52[1] net52[0] net53[31] net53[30] net53[29] net53[28] net53[27] net53[26] net53[25]
+ net53[24] net53[23] net53[22] net53[21] net53[20] net53[19] net53[18] net53[17] net53[16] net53[15] net53[14]
+ net53[13] net53[12] net53[11] net53[10] net53[9] net53[8] net53[7] net53[6] net53[5] net53[4] net53[3]
+ net53[2] net53[1] net53[0] net38[31] net38[30] net38[29] net38[28] net38[27] net38[26] net38[25] net38[24]
+ net38[23] net38[22] net38[21] net38[20] net38[19] net38[18] net38[17] net38[16] net38[15] net38[14] net38[13]
+ net38[12] net38[11] net38[10] net38[9] net38[8] net38[7] net38[6] net38[5] net38[4] net38[3] net38[2]
+ net38[1] net38[0] net39[31] net39[30] net39[29] net39[28] net39[27] net39[26] net39[25] net39[24] net39[23]
+ net39[22] net39[21] net39[20] net39[19] net39[18] net39[17] net39[16] net39[15] net39[14] net39[13] net39[12]
+ net39[11] net39[10] net39[9] net39[8] net39[7] net39[6] net39[5] net39[4] net39[3] net39[2] net39[1] net39[0]
+ rv_hazard
x6 alu2_pc_select clk_p[1] reset_n[0] net38[31] net38[30] net38[29] net38[28] net38[27] net38[26]
+ net38[25] net38[24] net38[23] net38[22] net38[21] net38[20] net38[19] net38[18] net38[17] net38[16] net38[15]
+ net38[14] net38[13] net38[12] net38[11] net38[10] net38[9] net38[8] net38[7] net38[6] net38[5] net38[4]
+ net38[3] net38[2] net38[1] net38[0] net17[31] net17[30] net17[29] net17[28] net17[27] net17[26] net17[25]
+ net17[24] net17[23] net17[22] net17[21] net17[20] net17[19] net17[18] net17[17] net17[16] net17[15] net17[14]
+ net17[13] net17[12] net17[11] net17[10] net17[9] net17[8] net17[7] net17[6] net17[5] net17[4] net17[3]
+ net17[2] net17[1] net17[0] o_data_adr[31] o_data_adr[30] o_data_adr[29] o_data_adr[28] o_data_adr[27]
+ o_data_adr[26] o_data_adr[25] o_data_adr[24] o_data_adr[23] o_data_adr[22] o_data_adr[21] o_data_adr[20]
+ o_data_adr[19] o_data_adr[18] o_data_adr[17] o_data_adr[16] o_data_adr[15] o_data_adr[14] o_data_adr[13]
+ o_data_adr[12] o_data_adr[11] o_data_adr[10] o_data_adr[9] o_data_adr[8] o_data_adr[7] o_data_adr[6] o_data_adr[5]
+ o_data_adr[4] o_data_adr[3] o_data_adr[2] o_data_adr[1] o_data_adr[0] o_data_write net18[31] net18[30] net18[29]
+ net18[28] net18[27] net18[26] net18[25] net18[24] net18[23] net18[22] net18[21] net18[20] net18[19] net18[18]
+ net18[17] net18[16] net18[15] net18[14] net18[13] net18[12] net18[11] net18[10] net18[9] net18[8] net18[7]
+ net18[6] net18[5] net18[4] net18[3] net18[2] net18[1] net18[0] net33 net19 net32[4] net32[3] net32[2]
+ net32[1] net32[0] net20 net21[4] net21[3] net21[2] net21[1] net21[0] alu2_pc_target[31] alu2_pc_target[30]
+ alu2_pc_target[29] alu2_pc_target[28] alu2_pc_target[27] alu2_pc_target[26] alu2_pc_target[25] alu2_pc_target[24]
+ alu2_pc_target[23] alu2_pc_target[22] alu2_pc_target[21] alu2_pc_target[20] alu2_pc_target[19] alu2_pc_target[18]
+ alu2_pc_target[17] alu2_pc_target[16] alu2_pc_target[15] alu2_pc_target[14] alu2_pc_target[13] alu2_pc_target[12]
+ alu2_pc_target[11] alu2_pc_target[10] alu2_pc_target[9] alu2_pc_target[8] alu2_pc_target[7] alu2_pc_target[6]
+ alu2_pc_target[5] alu2_pc_target[4] alu2_pc_target[3] alu2_pc_target[2] alu2_pc_target[1] alu2_res_src[2]
+ alu2_res_src[1] alu2_res_src[0] net22 net23 o_data_wdata[31] o_data_wdata[30] o_data_wdata[29] o_data_wdata[28]
+ o_data_wdata[27] o_data_wdata[26] o_data_wdata[25] o_data_wdata[24] o_data_wdata[23] o_data_wdata[22]
+ o_data_wdata[21] o_data_wdata[20] o_data_wdata[19] o_data_wdata[18] o_data_wdata[17] o_data_wdata[16]
+ o_data_wdata[15] o_data_wdata[14] o_data_wdata[13] o_data_wdata[12] o_data_wdata[11] o_data_wdata[10]
+ o_data_wdata[9] o_data_wdata[8] o_data_wdata[7] o_data_wdata[6] o_data_wdata[5] o_data_wdata[4] o_data_wdata[3]
+ o_data_wdata[2] o_data_wdata[1] o_data_wdata[0] o_data_sel[3] o_data_sel[2] o_data_sel[1] o_data_sel[0] net24[30]
+ net24[29] net24[28] net24[27] net24[26] net24[25] net24[24] net24[23] net24[22] net24[21] net24[20] net24[19]
+ net24[18] net24[17] net24[16] net24[15] net24[14] net24[13] net24[12] net24[11] net24[10] net24[9] net24[8]
+ net24[7] net24[6] net24[5] net24[4] net24[3] net24[2] net24[1] net24[0] net25[30] net25[29] net25[28]
+ net25[27] net25[26] net25[25] net25[24] net25[23] net25[22] net25[21] net25[20] net25[19] net25[18] net25[17]
+ net25[16] net25[15] net25[14] net25[13] net25[12] net25[11] net25[10] net25[9] net25[8] net25[7] net25[6]
+ net25[5] net25[4] net25[3] net25[2] net25[1] net25[0] net34[2] net34[1] net34[0] alu2_to_trap net26[30]
+ net26[29] net26[28] net26[27] net26[26] net26[25] net26[24] net26[23] net26[22] net26[21] net26[20] net26[19]
+ net26[18] net26[17] net26[16] net26[15] net26[14] net26[13] net26[12] net26[11] net26[10] net26[9] net26[8]
+ net26[7] net26[6] net26[5] net26[4] net26[3] net26[2] net26[1] net26[0] alu1_res_src[2] alu1_res_src[1]
+ alu1_res_src[0] net40 net27[2] net27[1] net27[0] net28[4] net28[3] net28[2] net28[1] net28[0] net29 net43[31]
+ net43[30] net43[29] net43[28] net43[27] net43[26] net43[25] net43[24] net43[23] net43[22] net43[21] net43[20]
+ net43[19] net43[18] net43[17] net43[16] net43[15] net43[14] net43[13] net43[12] net43[11] net43[10] net43[9]
+ net43[8] net43[7] net43[6] net43[5] net43[4] net43[3] net43[2] net43[1] net43[0] i_csr_read i_csr_data[31]
+ i_csr_data[30] i_csr_data[29] i_csr_data[28] i_csr_data[27] i_csr_data[26] i_csr_data[25] i_csr_data[24]
+ i_csr_data[23] i_csr_data[22] i_csr_data[21] i_csr_data[20] i_csr_data[19] i_csr_data[18] i_csr_data[17]
+ i_csr_data[16] i_csr_data[15] i_csr_data[14] i_csr_data[13] i_csr_data[12] i_csr_data[11] i_csr_data[10]
+ i_csr_data[9] i_csr_data[8] i_csr_data[7] i_csr_data[6] i_csr_data[5] i_csr_data[4] i_csr_data[3] i_csr_data[2]
+ i_csr_data[1] i_csr_data[0] net48 net50 rv_alu2
x7 clk_p[1] net35 net34[2] net34[1] net34[0] net39[31] net39[30] net39[29] net39[28] net39[27]
+ net39[26] net39[25] net39[24] net39[23] net39[22] net39[21] net39[20] net39[19] net39[18] net39[17] net39[16]
+ net39[15] net39[14] net39[13] net39[12] net39[11] net39[10] net39[9] net39[8] net39[7] net39[6] net39[5]
+ net39[4] net39[3] net39[2] net39[1] net39[0] net37[31] net37[30] net37[29] net37[28] net37[27] net37[26]
+ net37[25] net37[24] net37[23] net37[22] net37[21] net37[20] net37[19] net37[18] net37[17] net37[16] net37[15]
+ net37[14] net37[13] net37[12] net37[11] net37[10] net37[9] net37[8] net37[7] net37[6] net37[5] net37[4]
+ net37[3] net37[2] net37[1] net37[0] net36[4] net36[3] net36[2] net36[1] net36[0] net33 net32[4] net32[3]
+ net32[2] net32[1] net32[0] alu2_res_src[2] i_data_rdata[31] i_data_rdata[30] i_data_rdata[29]
+ i_data_rdata[28] i_data_rdata[27] i_data_rdata[26] i_data_rdata[25] i_data_rdata[24] i_data_rdata[23]
+ i_data_rdata[22] i_data_rdata[21] i_data_rdata[20] i_data_rdata[19] i_data_rdata[18] i_data_rdata[17]
+ i_data_rdata[16] i_data_rdata[15] i_data_rdata[14] i_data_rdata[13] i_data_rdata[12] i_data_rdata[11]
+ i_data_rdata[10] i_data_rdata[9] i_data_rdata[8] i_data_rdata[7] i_data_rdata[6] i_data_rdata[5] i_data_rdata[4]
+ i_data_rdata[3] i_data_rdata[2] i_data_rdata[1] i_data_rdata[0] net51 rv_write
x201 alu2_res_src[2] o_data_write VSS VSS VCC VCC o_data_req sky130_fd_sc_hd__or2_1
x202 o_data_req net33 VSS VSS VCC VCC o_instr_issued sky130_fd_sc_hd__or2_1
* noconn i_data_ack
x8 clk_p[2] net49 reset_n[1] net47 net46 fetch_pc_change net45 net41 net44 net40 alu1_res_src[2]
+ net48 net55 net56 net2[4] net2[3] net2[2] net2[1] net2[0] net3[4] net3[3] net3[2] net3[1] net3[0]
+ net21[4] net21[3] net21[2] net21[1] net21[0] net51 rv_ctrl
x203 net50 net23 net22 net42 VSS VSS VCC VCC net56 sky130_fd_sc_hd__o31a_1
* noconn #net55
x204 net47 net46 VSS VSS VCC VCC o_csr_masked sky130_fd_sc_hd__or2_1
x9 dec_f3[2] VSS VSS VCC VCC net57 sky130_fd_sc_hd__inv_1
x10 net57 VSS VSS VCC VCC o_csr_imm_sel sky130_fd_sc_hd__inv_1
**.ends
.end
